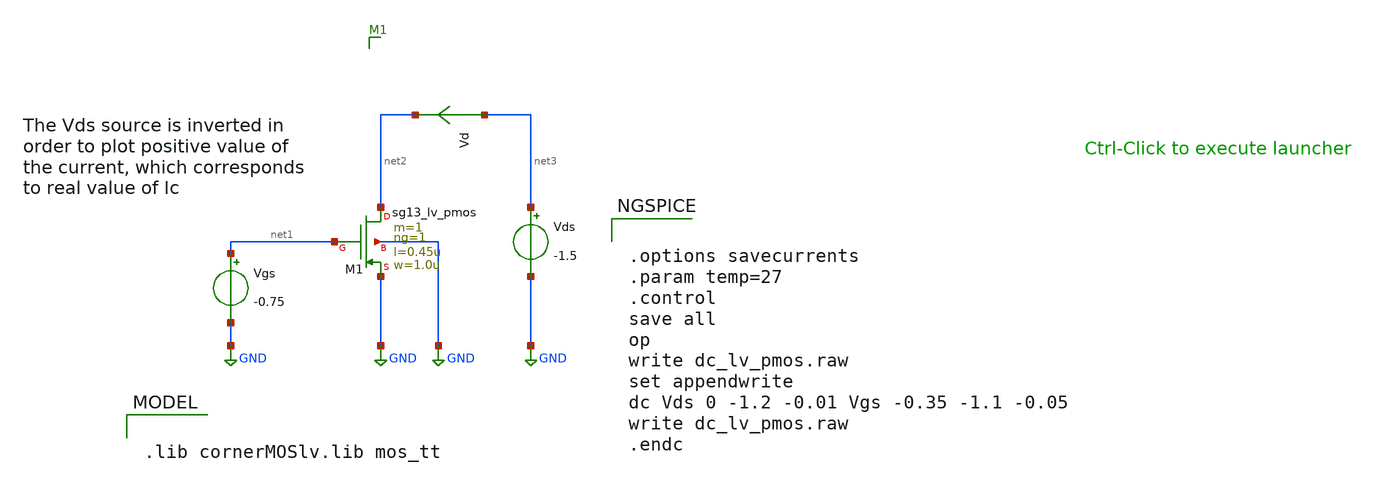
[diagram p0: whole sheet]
** sch_path: Modulo_Analogico/Lab1/dc_lv_pmos.sch
**.subckt dc_lv_pmos
Vgs net1 GND -0.75
Vds net3 GND -1.5
XM1 net2 net1 GND GND sg13_lv_pmos w=1.0u l=0.45u ng=1 m=1 mm_ok=1
Vd net3 net2 0
.save i(vd)
**** begin user architecture code

.lib cornerMOSlv.lib mos_tt



.options savecurrents
.param temp=27
.control
save all
op
write dc_lv_pmos.raw
set appendwrite
dc Vds 0 -1.2 -0.01 Vgs -0.35 -1.1 -0.05
write dc_lv_pmos.raw
.endc


**** end user architecture code
**.ends
.GLOBAL GND
.end
